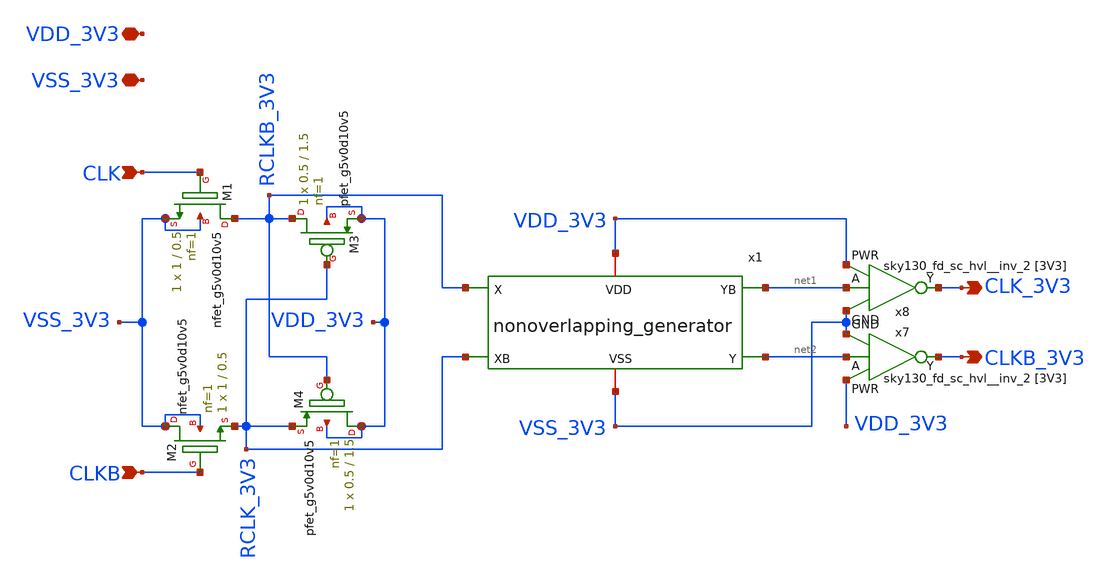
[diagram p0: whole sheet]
** sch_path: xschem/clock_3v3/clock_3v3.sch
**.subckt clock_3v3 CLK CLK_3V3 CLKB_3V3 VSS_3V3 VDD_3V3 CLKB
*.ipin CLK
*.opin CLK_3V3
*.opin CLKB_3V3
*.iopin VSS_3V3
*.iopin VDD_3V3
*.ipin CLKB
XM1 RCLKB_3V3 CLK VSS_3V3 VSS_3V3 sky130_fd_pr__nfet_g5v0d10v5 L=0.5 W=1 nf=1 ad='int((nf+1)/2) * W/nf * 0.29'
+ as='int((nf+2)/2) * W/nf * 0.29' pd='2*int((nf+1)/2) * (W/nf + 0.29)' ps='2*int((nf+2)/2) * (W/nf + 0.29)'
+ nrd='0.29 / W' nrs='0.29 / W' sa=0 sb=0 sd=0 mult=1 m=1
XM2 VSS_3V3 CLKB RCLK_3V3 VSS_3V3 sky130_fd_pr__nfet_g5v0d10v5 L=0.5 W=1 nf=1 ad='int((nf+1)/2) * W/nf * 0.29'
+ as='int((nf+2)/2) * W/nf * 0.29' pd='2*int((nf+1)/2) * (W/nf + 0.29)' ps='2*int((nf+2)/2) * (W/nf + 0.29)'
+ nrd='0.29 / W' nrs='0.29 / W' sa=0 sb=0 sd=0 mult=1 m=1
XM3 RCLKB_3V3 RCLK_3V3 VDD_3V3 VDD_3V3 sky130_fd_pr__pfet_g5v0d10v5 L=1.5 W=0.5 nf=1 ad='int((nf+1)/2) * W/nf * 0.29'
+ as='int((nf+2)/2) * W/nf * 0.29' pd='2*int((nf+1)/2) * (W/nf + 0.29)' ps='2*int((nf+2)/2) * (W/nf + 0.29)'
+ nrd='0.29 / W' nrs='0.29 / W' sa=0 sb=0 sd=0 mult=1 m=1
XM4 VDD_3V3 RCLKB_3V3 RCLK_3V3 VDD_3V3 sky130_fd_pr__pfet_g5v0d10v5 L=1.5 W=0.5 nf=1 ad='int((nf+1)/2) * W/nf * 0.29'
+ as='int((nf+2)/2) * W/nf * 0.29' pd='2*int((nf+1)/2) * (W/nf + 0.29)' ps='2*int((nf+2)/2) * (W/nf + 0.29)'
+ nrd='0.29 / W' nrs='0.29 / W' sa=0 sb=0 sd=0 mult=1 m=1
x7 net2 VSS_3V3 VSS_3V3 VDD_3V3 VDD_3V3 CLKB_3V3 sky130_fd_sc_hvl__inv_2
x8 net1 VSS_3V3 VSS_3V3 VDD_3V3 VDD_3V3 CLK_3V3 sky130_fd_sc_hvl__inv_2
x1 VDD_3V3 RCLKB_3V3 RCLK_3V3 VSS_3V3 net2 net1 nonoverlapping_generator
**.ends

* expanding   symbol:  clock_3v3/nonoverlapping_generator.sym # of pins=6
** sym_path: xschem/clock_3v3/nonoverlapping_generator.sym
** sch_path: xschem/clock_3v3/nonoverlapping_generator.sch
.subckt nonoverlapping_generator VDD X XB VSS Y YB
*.iopin VSS
*.iopin VDD
*.ipin X
*.ipin XB
*.opin YB
*.opin Y
XM1 YB X VDD VDD sky130_fd_pr__pfet_g5v0d10v5 L=0.5 W=0.5 nf=1 ad='int((nf+1)/2) * W/nf * 0.29' as='int((nf+2)/2) * W/nf * 0.29'
+ pd='2*int((nf+1)/2) * (W/nf + 0.29)' ps='2*int((nf+2)/2) * (W/nf + 0.29)' nrd='0.29 / W' nrs='0.29 / W'
+ sa=0 sb=0 sd=0 mult=1 m=1
XM2 net1 X YB VSS sky130_fd_pr__nfet_g5v0d10v5 L=0.5 W=1 nf=1 ad='int((nf+1)/2) * W/nf * 0.29' as='int((nf+2)/2) * W/nf * 0.29'
+ pd='2*int((nf+1)/2) * (W/nf + 0.29)' ps='2*int((nf+2)/2) * (W/nf + 0.29)' nrd='0.29 / W' nrs='0.29 / W'
+ sa=0 sb=0 sd=0 mult=1 m=1
XM3 YB Y VDD VDD sky130_fd_pr__pfet_g5v0d10v5 L=0.5 W=0.5 nf=1 ad='int((nf+1)/2) * W/nf * 0.29' as='int((nf+2)/2) * W/nf * 0.29'
+ pd='2*int((nf+1)/2) * (W/nf + 0.29)' ps='2*int((nf+2)/2) * (W/nf + 0.29)' nrd='0.29 / W' nrs='0.29 / W'
+ sa=0 sb=0 sd=0 mult=1 m=1
XM4 VSS Y net1 VSS sky130_fd_pr__nfet_g5v0d10v5 L=0.5 W=1 nf=1 ad='int((nf+1)/2) * W/nf * 0.29' as='int((nf+2)/2) * W/nf * 0.29'
+ pd='2*int((nf+1)/2) * (W/nf + 0.29)' ps='2*int((nf+2)/2) * (W/nf + 0.29)' nrd='0.29 / W' nrs='0.29 / W'
+ sa=0 sb=0 sd=0 mult=1 m=1
XM5 Y XB VDD VDD sky130_fd_pr__pfet_g5v0d10v5 L=0.5 W=0.5 nf=1 ad='int((nf+1)/2) * W/nf * 0.29' as='int((nf+2)/2) * W/nf * 0.29'
+ pd='2*int((nf+1)/2) * (W/nf + 0.29)' ps='2*int((nf+2)/2) * (W/nf + 0.29)' nrd='0.29 / W' nrs='0.29 / W'
+ sa=0 sb=0 sd=0 mult=1 m=1
XM6 net2 XB Y VSS sky130_fd_pr__nfet_g5v0d10v5 L=0.5 W=1 nf=1 ad='int((nf+1)/2) * W/nf * 0.29' as='int((nf+2)/2) * W/nf * 0.29'
+ pd='2*int((nf+1)/2) * (W/nf + 0.29)' ps='2*int((nf+2)/2) * (W/nf + 0.29)' nrd='0.29 / W' nrs='0.29 / W'
+ sa=0 sb=0 sd=0 mult=1 m=1
XM7 Y YB VDD VDD sky130_fd_pr__pfet_g5v0d10v5 L=0.5 W=0.5 nf=1 ad='int((nf+1)/2) * W/nf * 0.29' as='int((nf+2)/2) * W/nf * 0.29'
+ pd='2*int((nf+1)/2) * (W/nf + 0.29)' ps='2*int((nf+2)/2) * (W/nf + 0.29)' nrd='0.29 / W' nrs='0.29 / W'
+ sa=0 sb=0 sd=0 mult=1 m=1
XM8 VSS YB net2 VSS sky130_fd_pr__nfet_g5v0d10v5 L=0.5 W=1 nf=1 ad='int((nf+1)/2) * W/nf * 0.29' as='int((nf+2)/2) * W/nf * 0.29'
+ pd='2*int((nf+1)/2) * (W/nf + 0.29)' ps='2*int((nf+2)/2) * (W/nf + 0.29)' nrd='0.29 / W' nrs='0.29 / W'
+ sa=0 sb=0 sd=0 mult=1 m=1
.ends

.end
